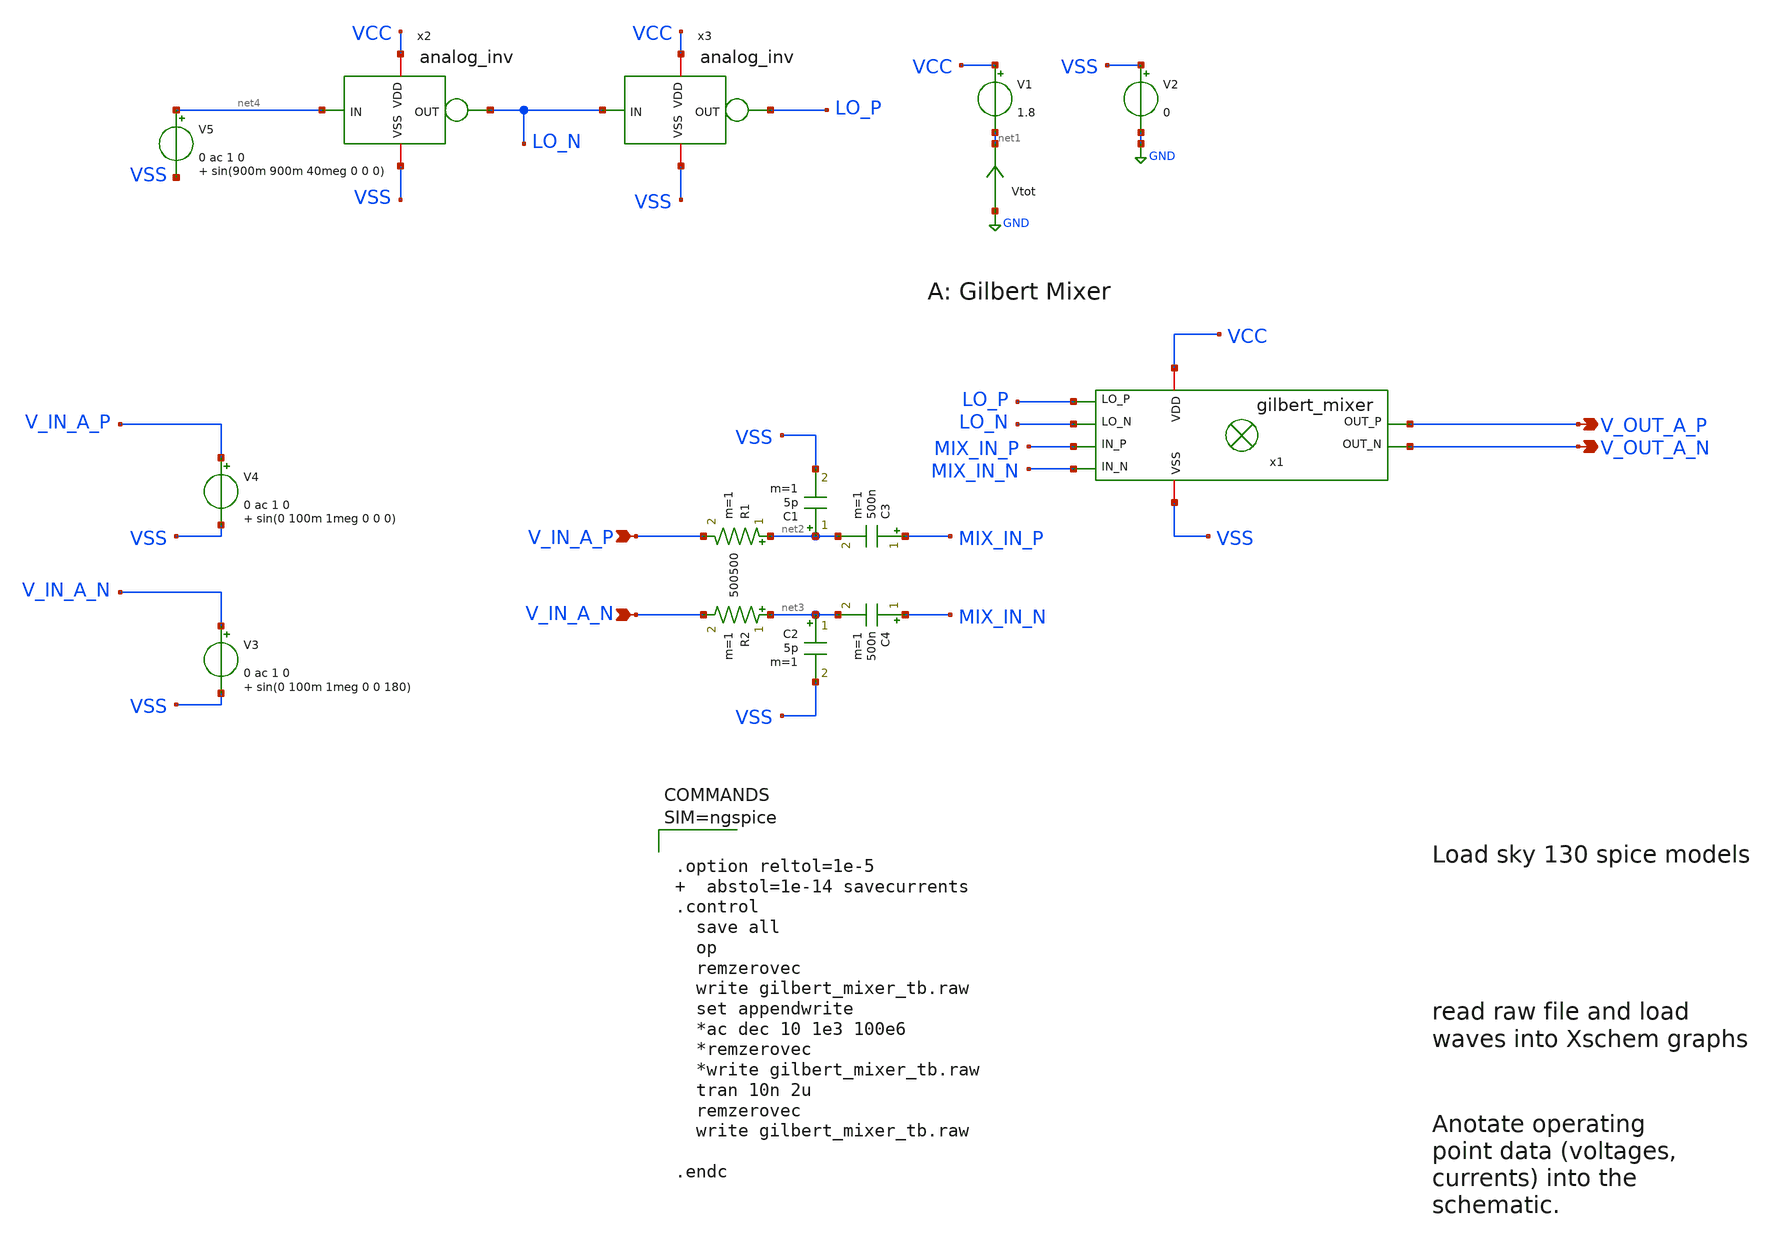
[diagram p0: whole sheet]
** sch_path: xschem/gilbert_mixer_tb.sch
**.subckt gilbert_mixer_tb V_IN_A_P V_OUT_A_N V_OUT_A_P V_IN_A_N
*.ipin V_IN_A_P
*.opin V_OUT_A_N
*.opin V_OUT_A_P
*.ipin V_IN_A_N
V1 VCC net1 1.8
V2 VSS GND 0
V4 V_IN_A_P VSS 0 ac 1 0 sin(0 100m 1meg 0 0 0)
R1 net2 V_IN_A_P 500 m=1
C1 net2 VSS 5p m=1
R2 net3 V_IN_A_N 500 m=1
C2 net3 VSS 5p m=1
x1 VSS VCC V_OUT_A_N V_OUT_A_P LO_N LO_P MIX_IN_N MIX_IN_P gilbert_mixer
V5 net4 VSS 0 ac 1 0 sin(900m 900m 40meg 0 0 0)
x2 VCC net4 LO_N VSS analog_inv
x3 VCC LO_N LO_P VSS analog_inv
V3 V_IN_A_N VSS 0 ac 1 0 sin(0 100m 1meg 0 0 180)
Vtot GND net1 0
.save i(vtot)
C3 MIX_IN_P net2 500n m=1
C4 MIX_IN_N net3 500n m=1
**** begin user architecture code

** opencircuitdesign pdks install
.lib $::SKYWATER_MODELS/sky130.lib.spice tt





.option reltol=1e-5   abstol=1e-14 savecurrents
.control
  save all
  op
  remzerovec
  write gilbert_mixer_tb.raw
  set appendwrite
  *ac dec 10 1e3 100e6
  *remzerovec
  *write gilbert_mixer_tb.raw
  tran 10n 2u
  remzerovec
  write gilbert_mixer_tb.raw

.endc



**** end user architecture code
**.ends

* expanding   symbol:  gilbert_mixer.sym # of pins=8
** sym_path: xschem/gilbert_mixer.sym
** sch_path: xschem/gilbert_mixer.sch
.subckt gilbert_mixer VSS VDD OUT_N OUT_P LO_N LO_P IN_N IN_P
*.ipin LO_P
*.ipin LO_N
*.ipin IN_P
*.ipin IN_N
*.opin OUT_N
*.opin OUT_P
*.iopin VDD
*.iopin VSS
XR3 VSS NET_R3 VSS sky130_fd_pr__res_high_po_0p35 L=0.1 mult=30 m=30
XM2 OUT_P IN_N NET_M6_DRAIN VSS sky130_fd_pr__nfet_01v8 L=0.38 W=3.6 nf=2 ad='int((nf+1)/2) * W/nf * 0.29'
+ as='int((nf+2)/2) * W/nf * 0.29' pd='2*int((nf+1)/2) * (W/nf + 0.29)' ps='2*int((nf+2)/2) * (W/nf + 0.29)'
+ nrd='0.29 / W' nrs='0.29 / W' sa=0 sb=0 sd=0 mult=1 m=1
XM4 OUT_N IN_N NET_M5_DRAIN VSS sky130_fd_pr__nfet_01v8 L=0.38 W=3.6 nf=2 ad='int((nf+1)/2) * W/nf * 0.29'
+ as='int((nf+2)/2) * W/nf * 0.29' pd='2*int((nf+1)/2) * (W/nf + 0.29)' ps='2*int((nf+2)/2) * (W/nf + 0.29)'
+ nrd='0.29 / W' nrs='0.29 / W' sa=0 sb=0 sd=0 mult=1 m=1
XM6 NET_M6_DRAIN LO_N NET_R3 VSS sky130_fd_pr__nfet_01v8 L=0.38 W=3.6 nf=2 ad='int((nf+1)/2) * W/nf * 0.29'
+ as='int((nf+2)/2) * W/nf * 0.29' pd='2*int((nf+1)/2) * (W/nf + 0.29)' ps='2*int((nf+2)/2) * (W/nf + 0.29)'
+ nrd='0.29 / W' nrs='0.29 / W' sa=0 sb=0 sd=0 mult=1 m=1
XM1 OUT_N IN_P NET_M6_DRAIN VSS sky130_fd_pr__nfet_01v8 L=0.38 W=3.6 nf=2 ad='int((nf+1)/2) * W/nf * 0.29'
+ as='int((nf+2)/2) * W/nf * 0.29' pd='2*int((nf+1)/2) * (W/nf + 0.29)' ps='2*int((nf+2)/2) * (W/nf + 0.29)'
+ nrd='0.29 / W' nrs='0.29 / W' sa=0 sb=0 sd=0 mult=1 m=1
XM3 OUT_P IN_P NET_M5_DRAIN VSS sky130_fd_pr__nfet_01v8 L=0.38 W=3.6 nf=2 ad='int((nf+1)/2) * W/nf * 0.29'
+ as='int((nf+2)/2) * W/nf * 0.29' pd='2*int((nf+1)/2) * (W/nf + 0.29)' ps='2*int((nf+2)/2) * (W/nf + 0.29)'
+ nrd='0.29 / W' nrs='0.29 / W' sa=0 sb=0 sd=0 mult=1 m=1
XM5 NET_M5_DRAIN LO_P NET_R3 VSS sky130_fd_pr__nfet_01v8 L=0.38 W=3.6 nf=2 ad='int((nf+1)/2) * W/nf * 0.29'
+ as='int((nf+2)/2) * W/nf * 0.29' pd='2*int((nf+1)/2) * (W/nf + 0.29)' ps='2*int((nf+2)/2) * (W/nf + 0.29)'
+ nrd='0.29 / W' nrs='0.29 / W' sa=0 sb=0 sd=0 mult=1 m=1
XR1 OUT_N VDD VSS sky130_fd_pr__res_high_po_0p35 L=15.3 mult=2 m=2
XR2 OUT_P VDD VSS sky130_fd_pr__res_high_po_0p35 L=15.3 mult=2 m=2
XR4 IN_N VDD VSS sky130_fd_pr__res_high_po_0p35 L=6 mult=2 m=2
XR5 VSS IN_N VSS sky130_fd_pr__res_high_po_0p35 L=7 mult=2 m=2
XR6 IN_P VDD VSS sky130_fd_pr__res_high_po_0p35 L=6 mult=2 m=2
XR7 VSS IN_P VSS sky130_fd_pr__res_high_po_0p35 L=7 mult=2 m=2
.ends


* expanding   symbol:  analog_inv.sym # of pins=4
** sym_path: xschem/analog_inv.sym
** sch_path: xschem/analog_inv.sch
.subckt analog_inv VDD IN OUT VSS
*.iopin VDD
*.iopin VSS
*.ipin IN
*.opin OUT
XM2 OUT IN VSS VSS sky130_fd_pr__nfet_01v8 L=0.38 W=3.6 nf=2 ad='int((nf+1)/2) * W/nf * 0.29' as='int((nf+2)/2) * W/nf * 0.29'
+ pd='2*int((nf+1)/2) * (W/nf + 0.29)' ps='2*int((nf+2)/2) * (W/nf + 0.29)' nrd='0.29 / W' nrs='0.29 / W'
+ sa=0 sb=0 sd=0 mult=1 m=1
XM1 OUT IN VDD VDD sky130_fd_pr__pfet_01v8 L=0.38 W=3.6 nf=2 ad='int((nf+1)/2) * W/nf * 0.29' as='int((nf+2)/2) * W/nf * 0.29'
+ pd='2*int((nf+1)/2) * (W/nf + 0.29)' ps='2*int((nf+2)/2) * (W/nf + 0.29)' nrd='0.29 / W' nrs='0.29 / W'
+ sa=0 sb=0 sd=0 mult=1 m=1
.ends

.GLOBAL GND
.end
